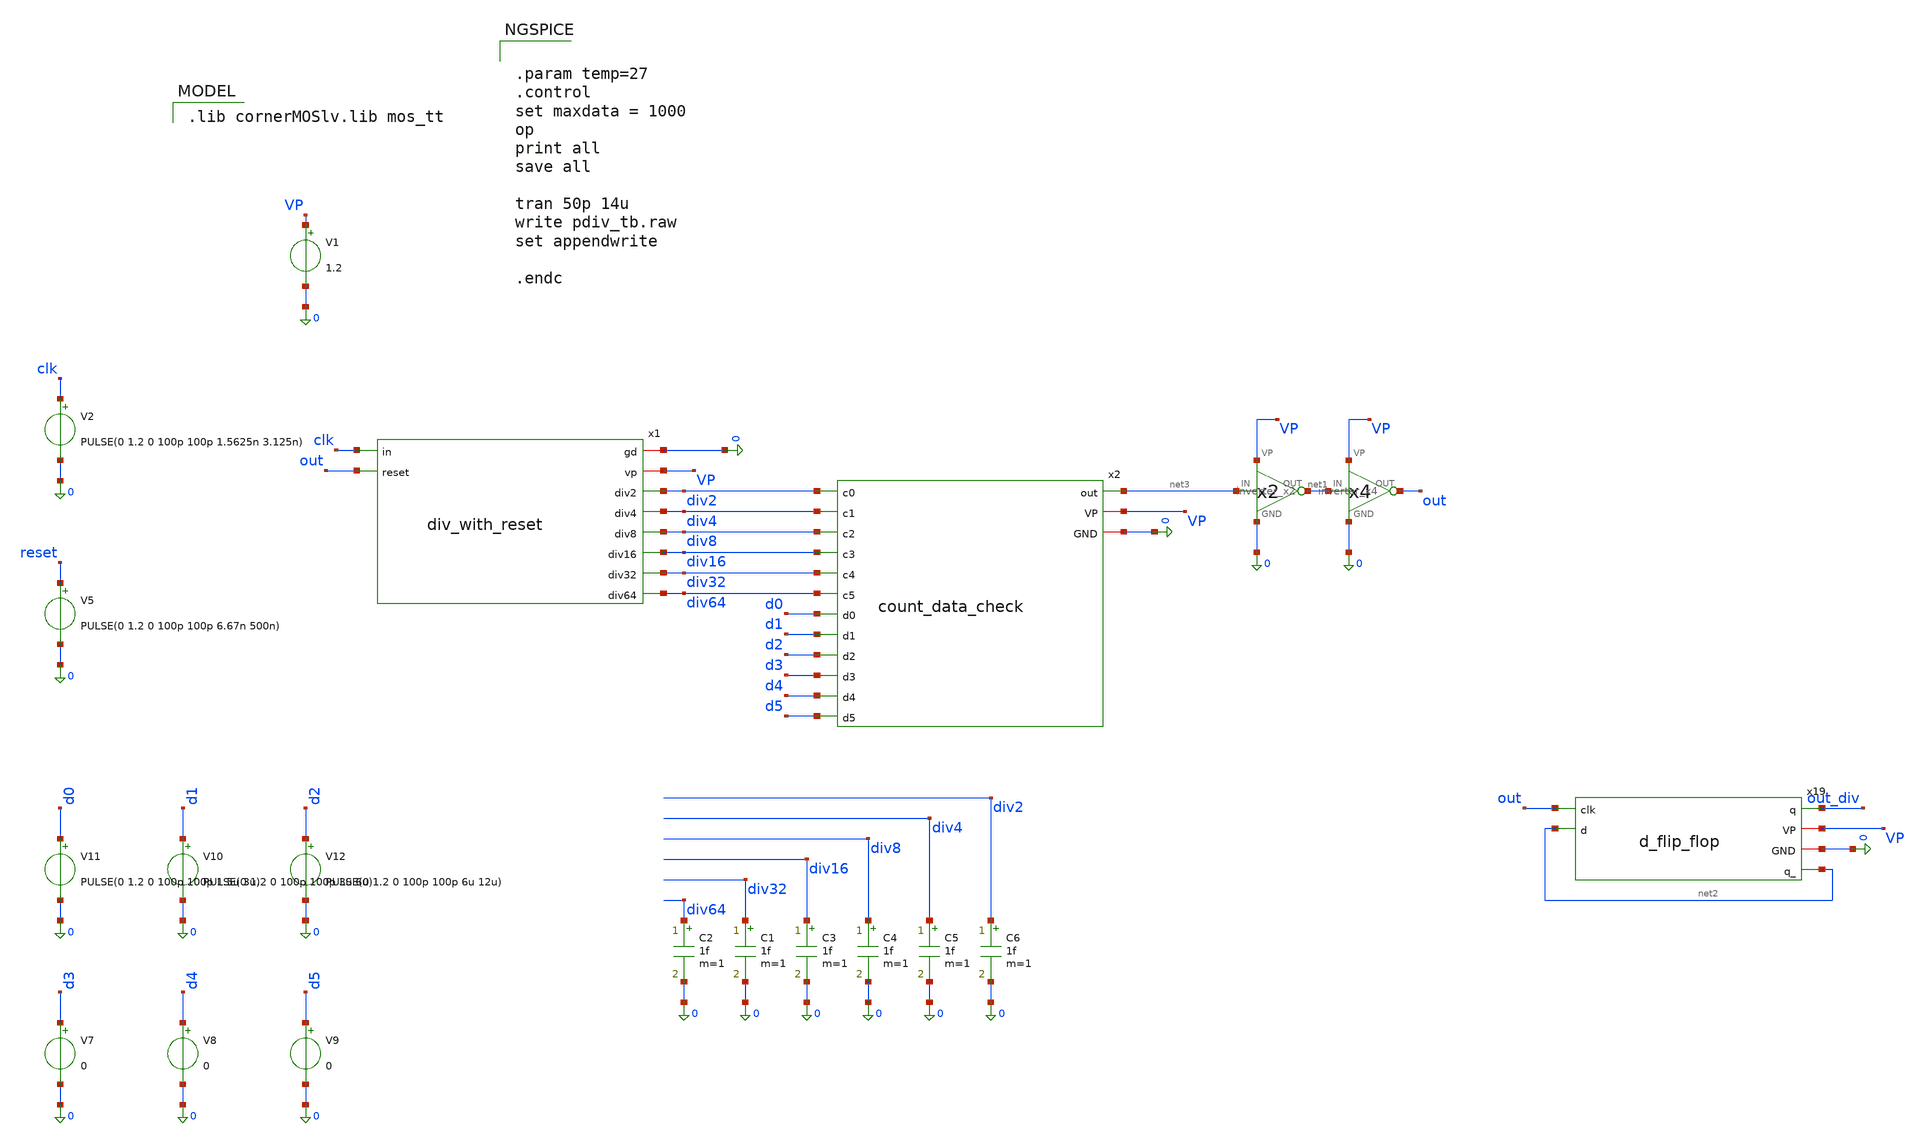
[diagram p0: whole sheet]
** sch_path: divider/tb/pdiv_sym_tb.sch
**.subckt pdiv_sym_tb
V1 VP 0 1.2
V2 clk 0 PULSE(0 1.2 0 100p 100p 1.5625n 3.125n)
x1 0 VP clk out div2 div4 div8 div16 div32 div64 div_with_reset
x2 net3 VP 0 div2 div4 div8 div16 div32 div64 d0 d1 d2 d3 d4 d5 count_data_check
C2 div64 0 1f m=1
C1 div32 0 1f m=1
C3 div16 0 1f m=1
C4 div8 0 1f m=1
C5 div4 0 1f m=1
C6 div2 0 1f m=1
V5 reset 0 PULSE(0 1.2 0 100p 100p 6.67n 500n)
x7 net3 net1 VP 0 inverter_x2
x8 net1 out VP 0 inverter_x4
x19 out_div VP 0 net2 out net2 d_flip_flop
V7 d3 0 0
V8 d4 0 0
V9 d5 0 0
V10 d1 0 PULSE(0 1.2 0 100p 100p 3u 6u)
V11 d0 0 PULSE(0 1.2 0 100p 100p 1.5u 3u)
V12 d2 0 PULSE(0 1.2 0 100p 100p 6u 12u)
**** begin user architecture code
 .lib cornerMOSlv.lib mos_tt



.param temp=27
.control
set maxdata = 1000
op
print all
save all

tran 50p 14u
write pdiv_tb.raw
set appendwrite

.endc


**** end user architecture code
**.ends
.end
